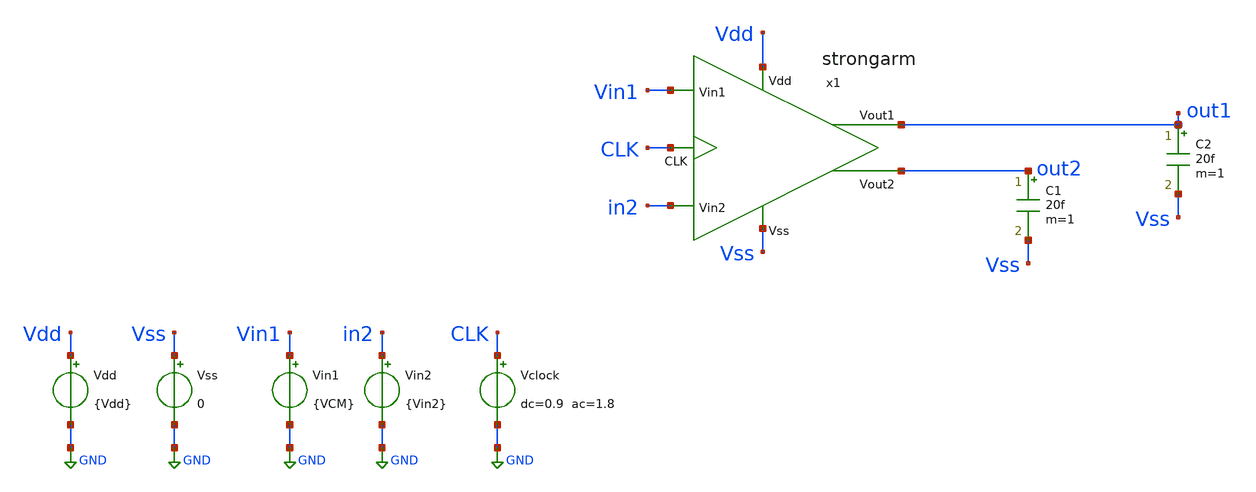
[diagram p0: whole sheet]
** sch_path: xschem/TB/TB_Op_SA.sch
**.subckt TB_Op_SA
Vdd Vdd GND {Vdd}
x1 out2 out1 Vdd Vss in2 Vin1 CLK strongarm
Vss Vss GND 0
C1 out2 Vss 20f m=1
C2 out1 Vss 20f m=1
Vin1 Vin1 GND {VCM}
Vin2 in2 GND {Vin2}
Vclock CLK GND dc=0.9 ac=1.8
**** begin user architecture code


.control
save all  @n.x1.xm3.nsg13_lv_nmos[gm]  @n.x1.xm4.nsg13_lv_nmos[gm]  @n.x1.xm3.nsg13_lv_nmos[ids]
+  @n.x1.xm4.nsg13_lv_nmos[ids]
*  @n.x1.xm8.nsg13_lv_pmos[ids]
op
let id3 = @n.x1.xm3.nsg13_lv_nmos[ids]
let id4 = @n.x1.xm4.nsg13_lv_nmos[ids]
let id8 = @n.x1.xm8.nsg13_lv_pmos[ids]

let gm3 = @n.x1.xm3.nsg13_lv_nmos[gm]
let gm4 = @n.x1.xm4.nsg13_lv_nmos[gm]
print id8 id3 id4
print gm3 gm4
.endc




.param Vdd   = 1.8
.param VCM   = 0.9
.param Vstep = 10m
.param Vin2  = VCM-Vstep
.ic V(out1) = 1.8
.ic V(out2) = 1.8
.ic V(x1.common) = 1.8
.ic V(x1.P) = 1.8
.ic V(x1.Q) = 1.8





.lib cornerMOSlv.lib mos_tt




** TRANSISTORES NMOS

.param W12 = 2.5u
.param L12 = 0.5u
.param M12 = 8
.param F12 = 5

.param W34 = 2u
.param L34 = 0.13u
.param M34 = 4
.param F34 = 2

.param W56 = 3.5u
.param L56 = 0.13u
.param M56 = 1
.param F56 = 7

.param W7  = 2.5u
.param L7  = 0.13u
.param M7  = 6
.param F7  = 5

.param W89 = 2u
.param L89 = 0.13u
.param M89 = 1
.param F89 = 4

.param Wab = 3u
.param Lab = 0.13u
.param Mab = 1
.param Fab = 6


**** end user architecture code
**.ends

* expanding   symbol:  proyecto-IPD413/xschem/sch/strongarm.sym # of pins=7
** sym_path: xschem/sch/strongarm.sym
** sch_path: xschem/sch/strongarm.sch
.subckt strongarm Vout2 Vout1 Vdd Vss Vin2 Vin1 CLK
*.opin Vout2
*.opin Vout1
*.ipin Vin1
*.ipin Vin2
*.ipin CLK
*.ipin Vss
*.ipin Vdd
XM1 common Vin1 P Vss sg13_lv_nmos w={W12} l={L12} ng={F12} m={M12} mm_ok=1
XM2 common Vin2 Q Vss sg13_lv_nmos w={W12} l={L12} ng={F12} m={M12} mm_ok=1
XM3 P Vout2 Vout1 Vss sg13_lv_nmos w={W34} l={L34} ng={F34} m={M34} mm_ok=1
XM4 Q Vout1 Vout2 Vss sg13_lv_nmos w={W34} l={L34} ng={F34} m={M34} mm_ok=1
XM6 Vout2 Vout1 Vdd Vdd sg13_lv_pmos w={W56} l={L56} ng={F56} m={M56} mm_ok=1
XM5 Vout1 Vout2 Vdd Vdd sg13_lv_pmos w={W56} l={L56} ng={F56} m={M56} mm_ok=1
XM7 Vss CLK common Vss sg13_lv_nmos w={W7} l={L7} ng={F7} m={M7} mm_ok=1
XM8 P CLK Vdd Vdd sg13_lv_pmos w={W89} l={L89} ng={F89} m={M89} mm_ok=1
XM9 Q CLK Vdd Vdd sg13_lv_pmos w={W89} l={L89} ng={F89} m={M89} mm_ok=1
XM11 Vdd CLK Vout2 Vdd sg13_lv_pmos w={Wab} l={Lab} ng={Fab} m={Mab} mm_ok=1
XM10 Vdd CLK Vout1 Vdd sg13_lv_pmos w={Wab} l={Lab} ng={Fab} m={Mab} mm_ok=1
.ends

.GLOBAL GND
.end
